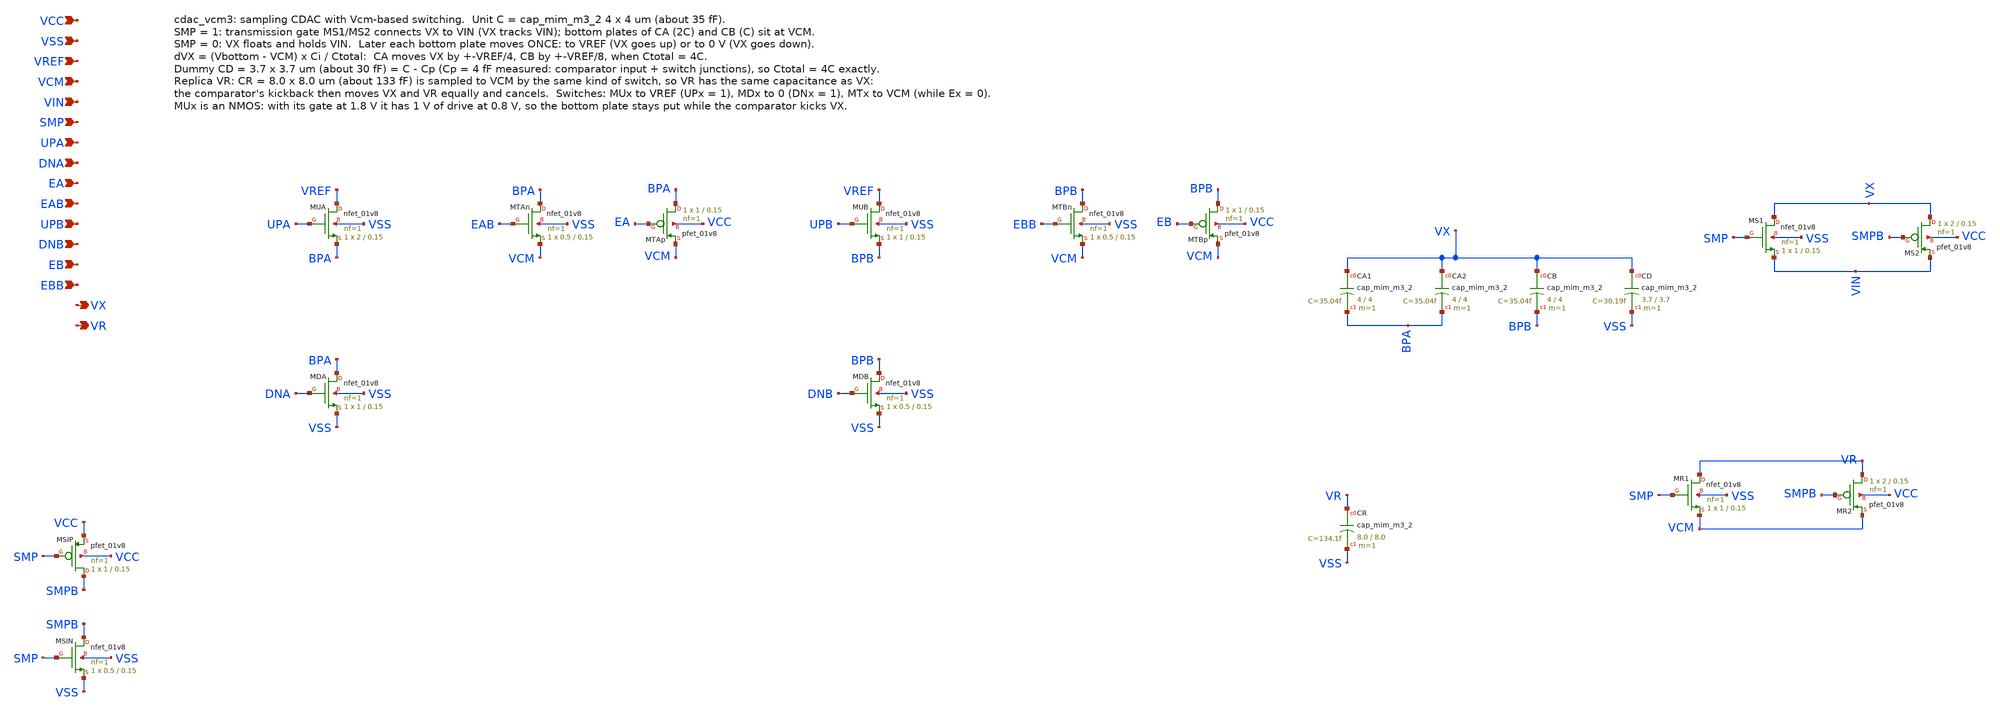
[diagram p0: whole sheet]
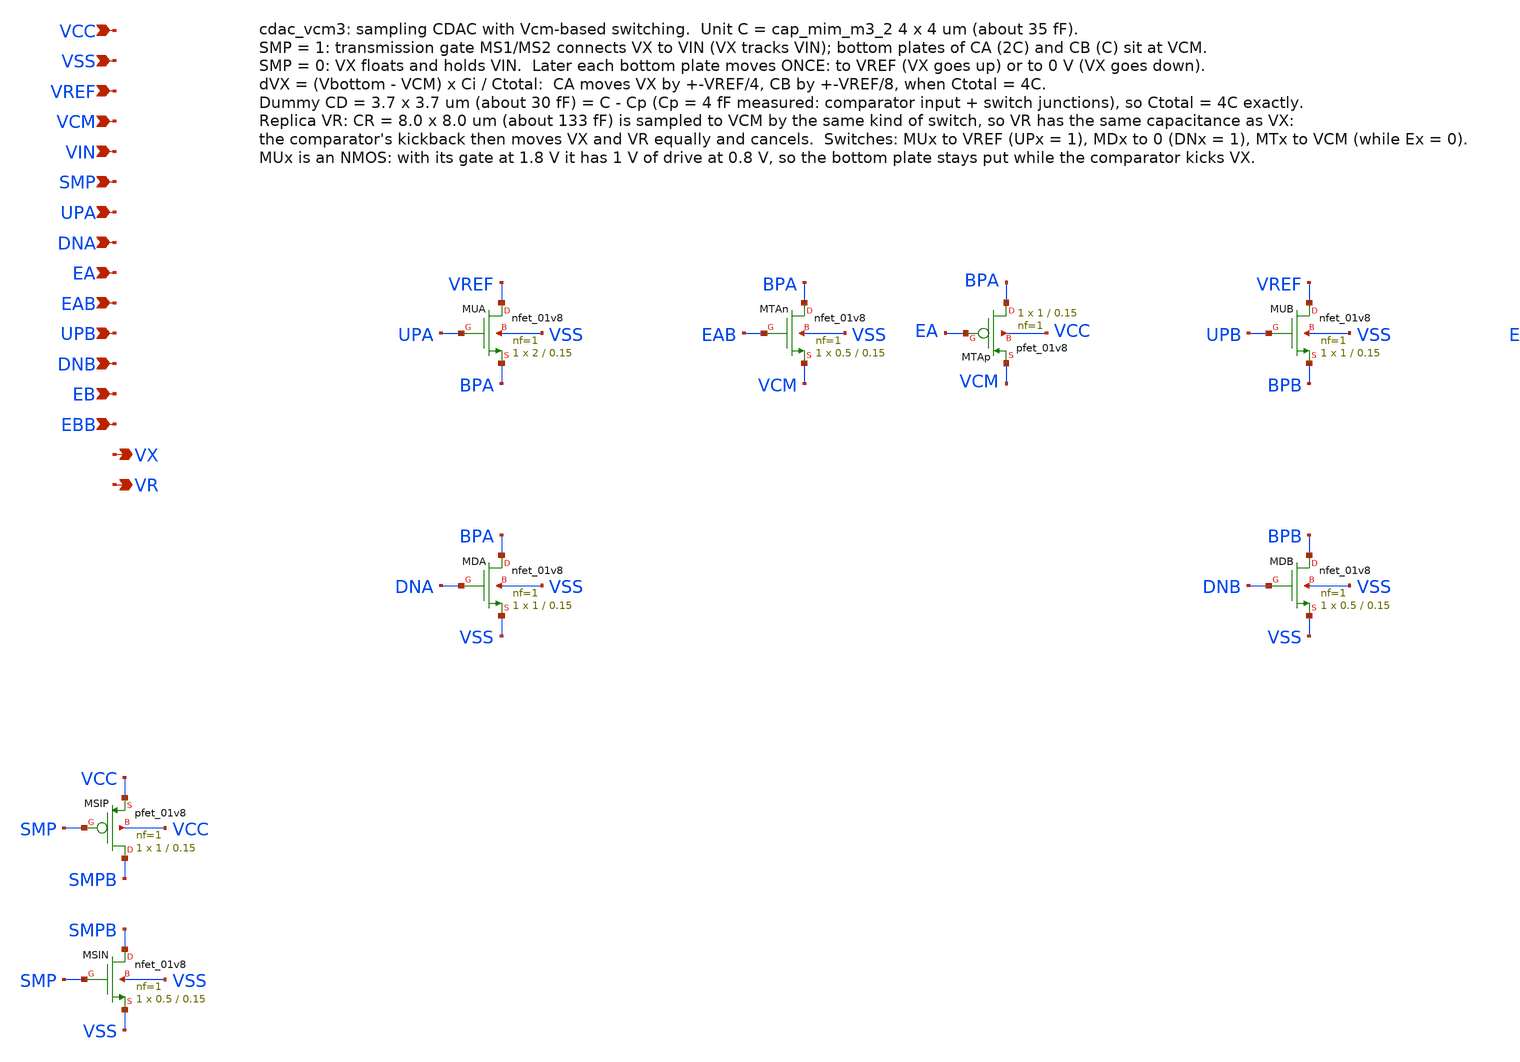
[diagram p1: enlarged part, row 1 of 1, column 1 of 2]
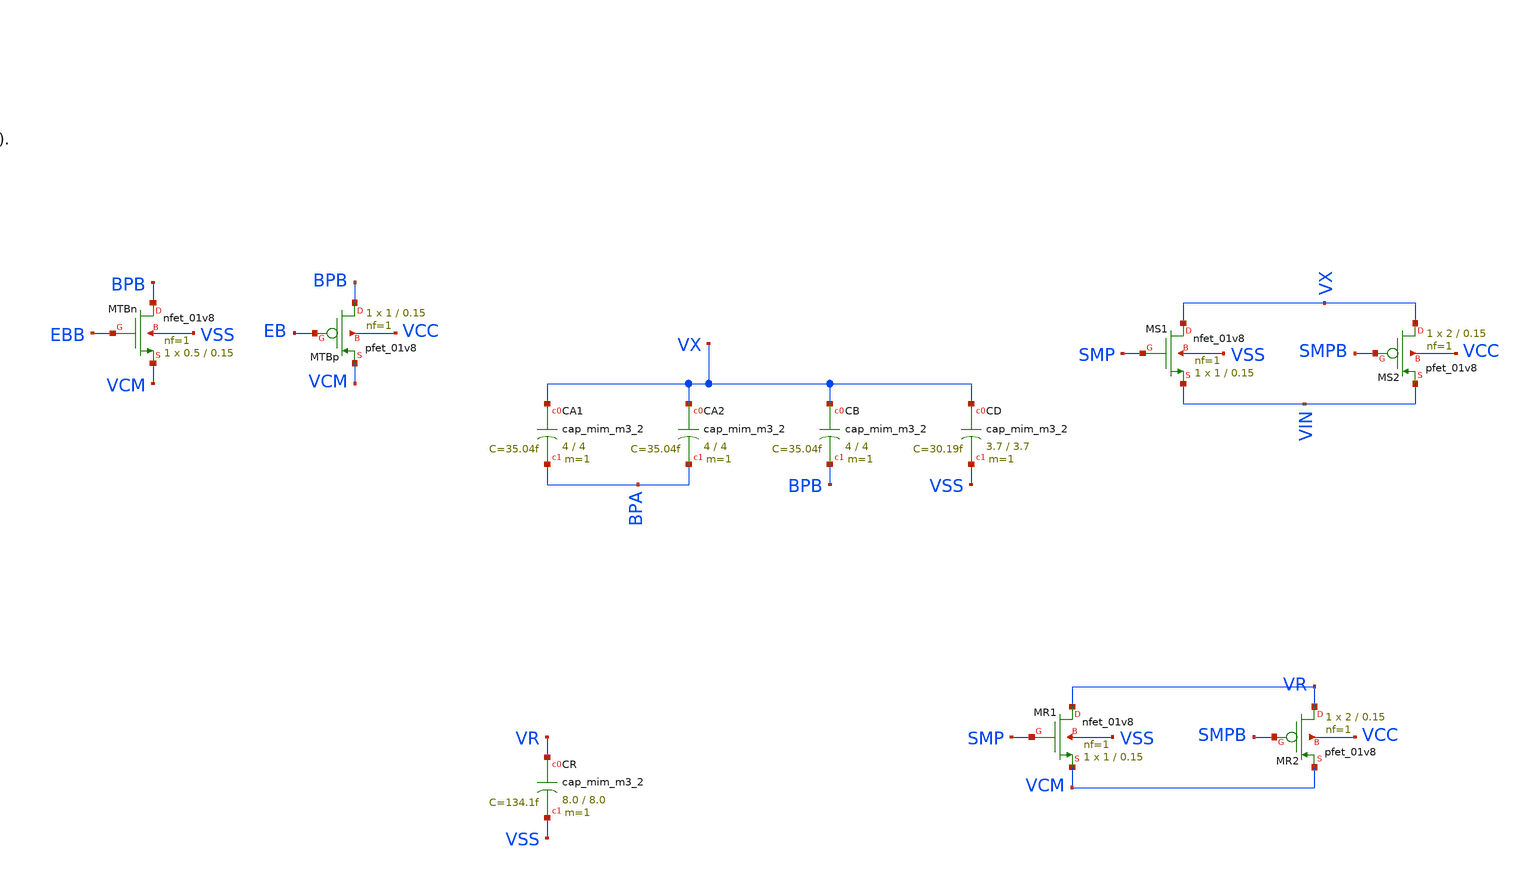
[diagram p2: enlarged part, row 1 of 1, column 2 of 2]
** sch_path: SAR_improved/cdac_vcm3.sch
**.subckt cdac_vcm3 VCC VSS VREF VCM VIN SMP UPA DNA EA EAB UPB DNB EB EBB VX VR
*.ipin VCC
*.ipin VSS
*.ipin VREF
*.ipin VCM
*.ipin VIN
*.ipin SMP
*.ipin UPA
*.ipin DNA
*.ipin EA
*.ipin EAB
*.ipin UPB
*.ipin DNB
*.ipin EB
*.ipin EBB
*.opin VX
*.opin VR
XMS1 VX SMP VIN VSS sky130_fd_pr__nfet_01v8 L=0.15 W=1 nf=1 ad='int((nf+1)/2) * W/nf * 0.29' as='int((nf+2)/2) * W/nf * 0.29'
+ pd='2*int((nf+1)/2) * (W/nf + 0.29)' ps='2*int((nf+2)/2) * (W/nf + 0.29)' nrd='0.29 / W' nrs='0.29 / W'
+ sa=0 sb=0 sd=0 mult=1 m=1
XMS2 VX SMPB VIN VCC sky130_fd_pr__pfet_01v8 L=0.15 W=2 nf=1 ad='int((nf+1)/2) * W/nf * 0.29' as='int((nf+2)/2) * W/nf * 0.29'
+ pd='2*int((nf+1)/2) * (W/nf + 0.29)' ps='2*int((nf+2)/2) * (W/nf + 0.29)' nrd='0.29 / W' nrs='0.29 / W'
+ sa=0 sb=0 sd=0 mult=1 m=1
XMR1 VR SMP VCM VSS sky130_fd_pr__nfet_01v8 L=0.15 W=1 nf=1 ad='int((nf+1)/2) * W/nf * 0.29' as='int((nf+2)/2) * W/nf * 0.29'
+ pd='2*int((nf+1)/2) * (W/nf + 0.29)' ps='2*int((nf+2)/2) * (W/nf + 0.29)' nrd='0.29 / W' nrs='0.29 / W'
+ sa=0 sb=0 sd=0 mult=1 m=1
XMR2 VR SMPB VCM VCC sky130_fd_pr__pfet_01v8 L=0.15 W=2 nf=1 ad='int((nf+1)/2) * W/nf * 0.29' as='int((nf+2)/2) * W/nf * 0.29'
+ pd='2*int((nf+1)/2) * (W/nf + 0.29)' ps='2*int((nf+2)/2) * (W/nf + 0.29)' nrd='0.29 / W' nrs='0.29 / W'
+ sa=0 sb=0 sd=0 mult=1 m=1
XMSIP SMPB SMP VCC VCC sky130_fd_pr__pfet_01v8 L=0.15 W=1 nf=1 ad='int((nf+1)/2) * W/nf * 0.29' as='int((nf+2)/2) * W/nf * 0.29'
+ pd='2*int((nf+1)/2) * (W/nf + 0.29)' ps='2*int((nf+2)/2) * (W/nf + 0.29)' nrd='0.29 / W' nrs='0.29 / W'
+ sa=0 sb=0 sd=0 mult=1 m=1
XMSIN SMPB SMP VSS VSS sky130_fd_pr__nfet_01v8 L=0.15 W=0.5 nf=1 ad='int((nf+1)/2) * W/nf * 0.29' as='int((nf+2)/2) * W/nf * 0.29'
+ pd='2*int((nf+1)/2) * (W/nf + 0.29)' ps='2*int((nf+2)/2) * (W/nf + 0.29)' nrd='0.29 / W' nrs='0.29 / W'
+ sa=0 sb=0 sd=0 mult=1 m=1
XMUA VREF UPA BPA VSS sky130_fd_pr__nfet_01v8 L=0.15 W=2 nf=1 ad='int((nf+1)/2) * W/nf * 0.29' as='int((nf+2)/2) * W/nf * 0.29'
+ pd='2*int((nf+1)/2) * (W/nf + 0.29)' ps='2*int((nf+2)/2) * (W/nf + 0.29)' nrd='0.29 / W' nrs='0.29 / W'
+ sa=0 sb=0 sd=0 mult=1 m=1
XMDA BPA DNA VSS VSS sky130_fd_pr__nfet_01v8 L=0.15 W=1 nf=1 ad='int((nf+1)/2) * W/nf * 0.29' as='int((nf+2)/2) * W/nf * 0.29'
+ pd='2*int((nf+1)/2) * (W/nf + 0.29)' ps='2*int((nf+2)/2) * (W/nf + 0.29)' nrd='0.29 / W' nrs='0.29 / W'
+ sa=0 sb=0 sd=0 mult=1 m=1
XMTAn BPA EAB VCM VSS sky130_fd_pr__nfet_01v8 L=0.15 W=0.5 nf=1 ad='int((nf+1)/2) * W/nf * 0.29' as='int((nf+2)/2) * W/nf * 0.29'
+ pd='2*int((nf+1)/2) * (W/nf + 0.29)' ps='2*int((nf+2)/2) * (W/nf + 0.29)' nrd='0.29 / W' nrs='0.29 / W'
+ sa=0 sb=0 sd=0 mult=1 m=1
XMTAp BPA EA VCM VCC sky130_fd_pr__pfet_01v8 L=0.15 W=1 nf=1 ad='int((nf+1)/2) * W/nf * 0.29' as='int((nf+2)/2) * W/nf * 0.29'
+ pd='2*int((nf+1)/2) * (W/nf + 0.29)' ps='2*int((nf+2)/2) * (W/nf + 0.29)' nrd='0.29 / W' nrs='0.29 / W'
+ sa=0 sb=0 sd=0 mult=1 m=1
XMUB VREF UPB BPB VSS sky130_fd_pr__nfet_01v8 L=0.15 W=1 nf=1 ad='int((nf+1)/2) * W/nf * 0.29' as='int((nf+2)/2) * W/nf * 0.29'
+ pd='2*int((nf+1)/2) * (W/nf + 0.29)' ps='2*int((nf+2)/2) * (W/nf + 0.29)' nrd='0.29 / W' nrs='0.29 / W'
+ sa=0 sb=0 sd=0 mult=1 m=1
XMDB BPB DNB VSS VSS sky130_fd_pr__nfet_01v8 L=0.15 W=0.5 nf=1 ad='int((nf+1)/2) * W/nf * 0.29' as='int((nf+2)/2) * W/nf * 0.29'
+ pd='2*int((nf+1)/2) * (W/nf + 0.29)' ps='2*int((nf+2)/2) * (W/nf + 0.29)' nrd='0.29 / W' nrs='0.29 / W'
+ sa=0 sb=0 sd=0 mult=1 m=1
XMTBn BPB EBB VCM VSS sky130_fd_pr__nfet_01v8 L=0.15 W=0.5 nf=1 ad='int((nf+1)/2) * W/nf * 0.29' as='int((nf+2)/2) * W/nf * 0.29'
+ pd='2*int((nf+1)/2) * (W/nf + 0.29)' ps='2*int((nf+2)/2) * (W/nf + 0.29)' nrd='0.29 / W' nrs='0.29 / W'
+ sa=0 sb=0 sd=0 mult=1 m=1
XMTBp BPB EB VCM VCC sky130_fd_pr__pfet_01v8 L=0.15 W=1 nf=1 ad='int((nf+1)/2) * W/nf * 0.29' as='int((nf+2)/2) * W/nf * 0.29'
+ pd='2*int((nf+1)/2) * (W/nf + 0.29)' ps='2*int((nf+2)/2) * (W/nf + 0.29)' nrd='0.29 / W' nrs='0.29 / W'
+ sa=0 sb=0 sd=0 mult=1 m=1
XCA1 VX BPA sky130_fd_pr__cap_mim_m3_2 W=4 L=4 MF=1 m=1
XCA2 VX BPA sky130_fd_pr__cap_mim_m3_2 W=4 L=4 MF=1 m=1
XCB VX BPB sky130_fd_pr__cap_mim_m3_2 W=4 L=4 MF=1 m=1
XCD VX VSS sky130_fd_pr__cap_mim_m3_2 W=3.7 L=3.7 MF=1 m=1
XCR VR VSS sky130_fd_pr__cap_mim_m3_2 W=8.0 L=8.0 MF=1 m=1
**.ends
.end
